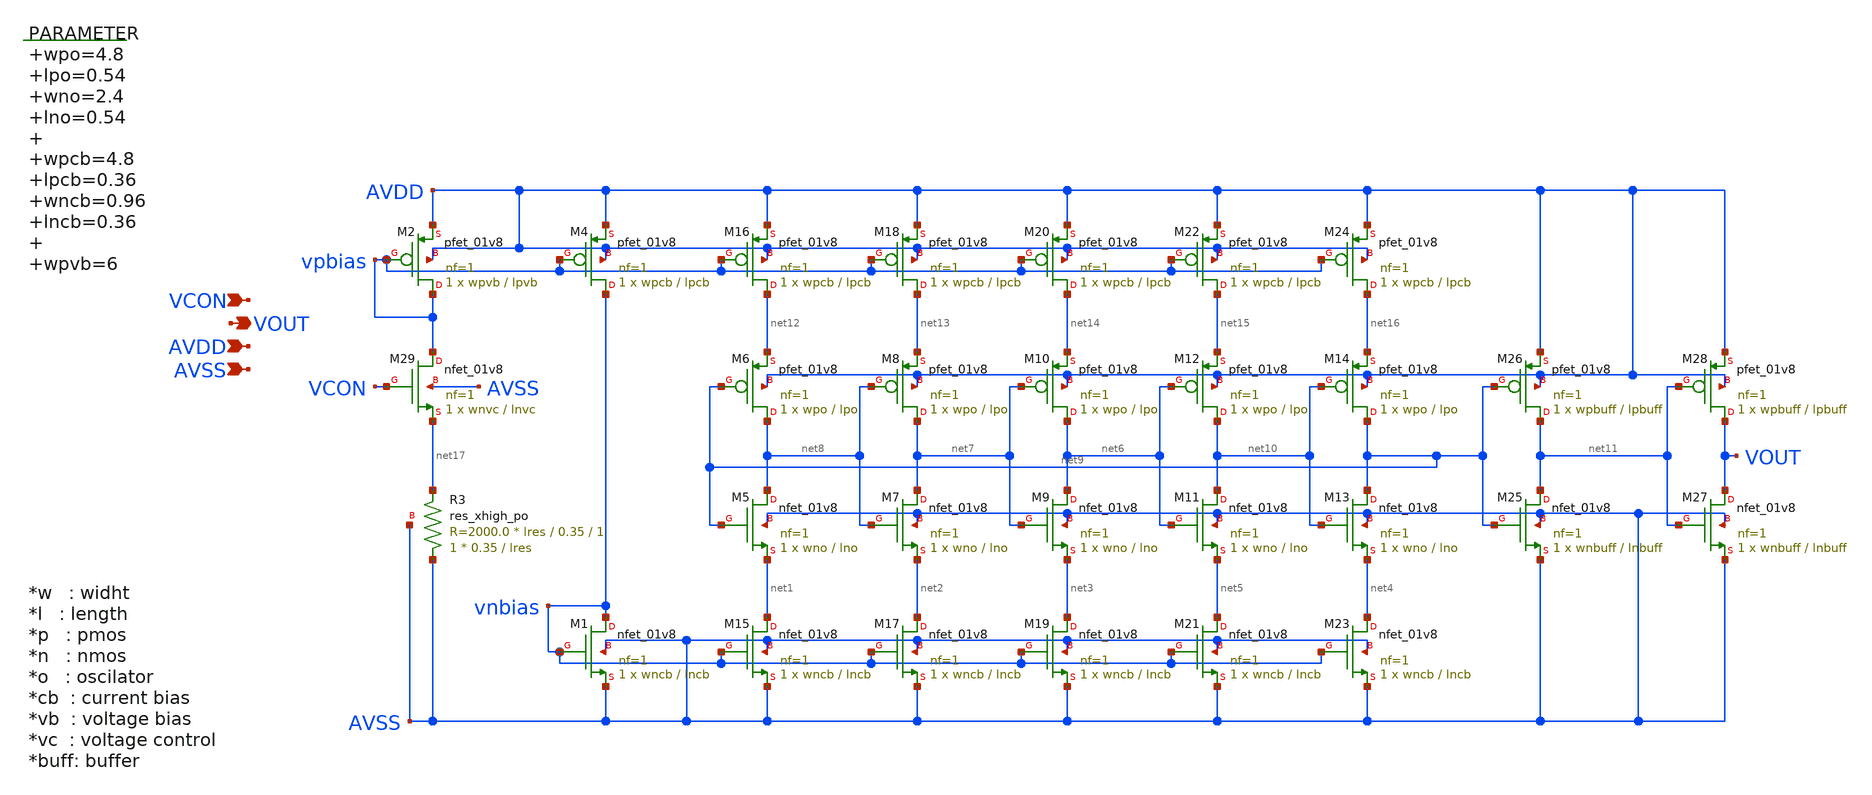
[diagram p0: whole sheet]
** sch_path: xschem/vco.sch
**.subckt vco VCON VOUT AVDD AVSS
*.ipin VCON
*.opin VOUT
*.ipin AVDD
*.ipin AVSS
.param wpo=4.8 lpo=0.54 wno=2.4 lno=0.54 wpcb=4.8 lpcb=0.36 wncb=0.96 lncb=0.36 wpvb=6 lpvb=0.9
+ wnvc=96 lnvc=0.9 wpbuff=4.8 lpbuff=0.18 wnbuff=1.2 lnbuff=0.18 lres=3.5

XM1 vnbias vnbias AVSS AVSS sky130_fd_pr__nfet_01v8 L=lncb W=wncb nf=1 ad='int((nf+1)/2) * W/nf * 0.29'
+ as='int((nf+2)/2) * W/nf * 0.29' pd='2*int((nf+1)/2) * (W/nf + 0.29)' ps='2*int((nf+2)/2) * (W/nf + 0.29)'
+ nrd='0.29 / W' nrs='0.29 / W' sa=0 sb=0 sd=0 mult=1 m=1
XM2 vpbias vpbias AVDD AVDD sky130_fd_pr__pfet_01v8 L=lpvb W=wpvb nf=1 ad='int((nf+1)/2) * W/nf * 0.29'
+ as='int((nf+2)/2) * W/nf * 0.29' pd='2*int((nf+1)/2) * (W/nf + 0.29)' ps='2*int((nf+2)/2) * (W/nf + 0.29)'
+ nrd='0.29 / W' nrs='0.29 / W' sa=0 sb=0 sd=0 mult=1 m=1
XM4 vnbias vpbias AVDD AVDD sky130_fd_pr__pfet_01v8 L=lpcb W=wpcb nf=1 ad='int((nf+1)/2) * W/nf * 0.29'
+ as='int((nf+2)/2) * W/nf * 0.29' pd='2*int((nf+1)/2) * (W/nf + 0.29)' ps='2*int((nf+2)/2) * (W/nf + 0.29)'
+ nrd='0.29 / W' nrs='0.29 / W' sa=0 sb=0 sd=0 mult=1 m=1
XM5 net8 net9 net1 AVSS sky130_fd_pr__nfet_01v8 L=lno W=wno nf=1 ad='int((nf+1)/2) * W/nf * 0.29' as='int((nf+2)/2) * W/nf * 0.29'
+ pd='2*int((nf+1)/2) * (W/nf + 0.29)' ps='2*int((nf+2)/2) * (W/nf + 0.29)' nrd='0.29 / W' nrs='0.29 / W'
+ sa=0 sb=0 sd=0 mult=1 m=1
XM6 net8 net9 net12 AVDD sky130_fd_pr__pfet_01v8 L=lpo W=wpo nf=1 ad='int((nf+1)/2) * W/nf * 0.29' as='int((nf+2)/2) * W/nf * 0.29'
+ pd='2*int((nf+1)/2) * (W/nf + 0.29)' ps='2*int((nf+2)/2) * (W/nf + 0.29)' nrd='0.29 / W' nrs='0.29 / W'
+ sa=0 sb=0 sd=0 mult=1 m=1
XM7 net7 net8 net2 AVSS sky130_fd_pr__nfet_01v8 L=lno W=wno nf=1 ad='int((nf+1)/2) * W/nf * 0.29' as='int((nf+2)/2) * W/nf * 0.29'
+ pd='2*int((nf+1)/2) * (W/nf + 0.29)' ps='2*int((nf+2)/2) * (W/nf + 0.29)' nrd='0.29 / W' nrs='0.29 / W'
+ sa=0 sb=0 sd=0 mult=1 m=1
XM8 net7 net8 net13 AVDD sky130_fd_pr__pfet_01v8 L=lpo W=wpo nf=1 ad='int((nf+1)/2) * W/nf * 0.29' as='int((nf+2)/2) * W/nf * 0.29'
+ pd='2*int((nf+1)/2) * (W/nf + 0.29)' ps='2*int((nf+2)/2) * (W/nf + 0.29)' nrd='0.29 / W' nrs='0.29 / W'
+ sa=0 sb=0 sd=0 mult=1 m=1
XM9 net6 net7 net3 AVSS sky130_fd_pr__nfet_01v8 L=lno W=wno nf=1 ad='int((nf+1)/2) * W/nf * 0.29' as='int((nf+2)/2) * W/nf * 0.29'
+ pd='2*int((nf+1)/2) * (W/nf + 0.29)' ps='2*int((nf+2)/2) * (W/nf + 0.29)' nrd='0.29 / W' nrs='0.29 / W'
+ sa=0 sb=0 sd=0 mult=1 m=1
XM10 net6 net7 net14 AVDD sky130_fd_pr__pfet_01v8 L=lpo W=wpo nf=1 ad='int((nf+1)/2) * W/nf * 0.29' as='int((nf+2)/2) * W/nf * 0.29'
+ pd='2*int((nf+1)/2) * (W/nf + 0.29)' ps='2*int((nf+2)/2) * (W/nf + 0.29)' nrd='0.29 / W' nrs='0.29 / W'
+ sa=0 sb=0 sd=0 mult=1 m=1
XM11 net10 net6 net5 AVSS sky130_fd_pr__nfet_01v8 L=lno W=wno nf=1 ad='int((nf+1)/2) * W/nf * 0.29' as='int((nf+2)/2) * W/nf * 0.29'
+ pd='2*int((nf+1)/2) * (W/nf + 0.29)' ps='2*int((nf+2)/2) * (W/nf + 0.29)' nrd='0.29 / W' nrs='0.29 / W'
+ sa=0 sb=0 sd=0 mult=1 m=1
XM12 net10 net6 net15 AVDD sky130_fd_pr__pfet_01v8 L=lpo W=wpo nf=1 ad='int((nf+1)/2) * W/nf * 0.29'
+ as='int((nf+2)/2) * W/nf * 0.29' pd='2*int((nf+1)/2) * (W/nf + 0.29)' ps='2*int((nf+2)/2) * (W/nf + 0.29)'
+ nrd='0.29 / W' nrs='0.29 / W' sa=0 sb=0 sd=0 mult=1 m=1
XM13 net9 net10 net4 AVSS sky130_fd_pr__nfet_01v8 L=lno W=wno nf=1 ad='int((nf+1)/2) * W/nf * 0.29' as='int((nf+2)/2) * W/nf * 0.29'
+ pd='2*int((nf+1)/2) * (W/nf + 0.29)' ps='2*int((nf+2)/2) * (W/nf + 0.29)' nrd='0.29 / W' nrs='0.29 / W'
+ sa=0 sb=0 sd=0 mult=1 m=1
XM14 net9 net10 net16 AVDD sky130_fd_pr__pfet_01v8 L=lpo W=wpo nf=1 ad='int((nf+1)/2) * W/nf * 0.29'
+ as='int((nf+2)/2) * W/nf * 0.29' pd='2*int((nf+1)/2) * (W/nf + 0.29)' ps='2*int((nf+2)/2) * (W/nf + 0.29)'
+ nrd='0.29 / W' nrs='0.29 / W' sa=0 sb=0 sd=0 mult=1 m=1
XM16 net12 vpbias AVDD AVDD sky130_fd_pr__pfet_01v8 L=lpcb W=wpcb nf=1 ad='int((nf+1)/2) * W/nf * 0.29'
+ as='int((nf+2)/2) * W/nf * 0.29' pd='2*int((nf+1)/2) * (W/nf + 0.29)' ps='2*int((nf+2)/2) * (W/nf + 0.29)'
+ nrd='0.29 / W' nrs='0.29 / W' sa=0 sb=0 sd=0 mult=1 m=1
XM18 net13 vpbias AVDD AVDD sky130_fd_pr__pfet_01v8 L=lpcb W=wpcb nf=1 ad='int((nf+1)/2) * W/nf * 0.29'
+ as='int((nf+2)/2) * W/nf * 0.29' pd='2*int((nf+1)/2) * (W/nf + 0.29)' ps='2*int((nf+2)/2) * (W/nf + 0.29)'
+ nrd='0.29 / W' nrs='0.29 / W' sa=0 sb=0 sd=0 mult=1 m=1
XM20 net14 vpbias AVDD AVDD sky130_fd_pr__pfet_01v8 L=lpcb W=wpcb nf=1 ad='int((nf+1)/2) * W/nf * 0.29'
+ as='int((nf+2)/2) * W/nf * 0.29' pd='2*int((nf+1)/2) * (W/nf + 0.29)' ps='2*int((nf+2)/2) * (W/nf + 0.29)'
+ nrd='0.29 / W' nrs='0.29 / W' sa=0 sb=0 sd=0 mult=1 m=1
XM22 net15 vpbias AVDD AVDD sky130_fd_pr__pfet_01v8 L=lpcb W=wpcb nf=1 ad='int((nf+1)/2) * W/nf * 0.29'
+ as='int((nf+2)/2) * W/nf * 0.29' pd='2*int((nf+1)/2) * (W/nf + 0.29)' ps='2*int((nf+2)/2) * (W/nf + 0.29)'
+ nrd='0.29 / W' nrs='0.29 / W' sa=0 sb=0 sd=0 mult=1 m=1
XM24 net16 vpbias AVDD AVDD sky130_fd_pr__pfet_01v8 L=lpcb W=wpcb nf=1 ad='int((nf+1)/2) * W/nf * 0.29'
+ as='int((nf+2)/2) * W/nf * 0.29' pd='2*int((nf+1)/2) * (W/nf + 0.29)' ps='2*int((nf+2)/2) * (W/nf + 0.29)'
+ nrd='0.29 / W' nrs='0.29 / W' sa=0 sb=0 sd=0 mult=1 m=1
XM25 net11 net9 AVSS AVSS sky130_fd_pr__nfet_01v8 L=lnbuff W=wnbuff nf=1 ad='int((nf+1)/2) * W/nf * 0.29'
+ as='int((nf+2)/2) * W/nf * 0.29' pd='2*int((nf+1)/2) * (W/nf + 0.29)' ps='2*int((nf+2)/2) * (W/nf + 0.29)'
+ nrd='0.29 / W' nrs='0.29 / W' sa=0 sb=0 sd=0 mult=1 m=1
XM26 net11 net9 AVDD AVDD sky130_fd_pr__pfet_01v8 L=lpbuff W=wpbuff nf=1 ad='int((nf+1)/2) * W/nf * 0.29'
+ as='int((nf+2)/2) * W/nf * 0.29' pd='2*int((nf+1)/2) * (W/nf + 0.29)' ps='2*int((nf+2)/2) * (W/nf + 0.29)'
+ nrd='0.29 / W' nrs='0.29 / W' sa=0 sb=0 sd=0 mult=1 m=1
XM27 VOUT net11 AVSS AVSS sky130_fd_pr__nfet_01v8 L=lnbuff W=wnbuff nf=1 ad='int((nf+1)/2) * W/nf * 0.29'
+ as='int((nf+2)/2) * W/nf * 0.29' pd='2*int((nf+1)/2) * (W/nf + 0.29)' ps='2*int((nf+2)/2) * (W/nf + 0.29)'
+ nrd='0.29 / W' nrs='0.29 / W' sa=0 sb=0 sd=0 mult=1 m=1
XM28 VOUT net11 AVDD AVDD sky130_fd_pr__pfet_01v8 L=lpbuff W=wpbuff nf=1 ad='int((nf+1)/2) * W/nf * 0.29'
+ as='int((nf+2)/2) * W/nf * 0.29' pd='2*int((nf+1)/2) * (W/nf + 0.29)' ps='2*int((nf+2)/2) * (W/nf + 0.29)'
+ nrd='0.29 / W' nrs='0.29 / W' sa=0 sb=0 sd=0 mult=1 m=1
XM15 net1 vnbias AVSS AVSS sky130_fd_pr__nfet_01v8 L=lncb W=wncb nf=1 ad='int((nf+1)/2) * W/nf * 0.29'
+ as='int((nf+2)/2) * W/nf * 0.29' pd='2*int((nf+1)/2) * (W/nf + 0.29)' ps='2*int((nf+2)/2) * (W/nf + 0.29)'
+ nrd='0.29 / W' nrs='0.29 / W' sa=0 sb=0 sd=0 mult=1 m=1
XM17 net2 vnbias AVSS AVSS sky130_fd_pr__nfet_01v8 L=lncb W=wncb nf=1 ad='int((nf+1)/2) * W/nf * 0.29'
+ as='int((nf+2)/2) * W/nf * 0.29' pd='2*int((nf+1)/2) * (W/nf + 0.29)' ps='2*int((nf+2)/2) * (W/nf + 0.29)'
+ nrd='0.29 / W' nrs='0.29 / W' sa=0 sb=0 sd=0 mult=1 m=1
XM19 net3 vnbias AVSS AVSS sky130_fd_pr__nfet_01v8 L=lncb W=wncb nf=1 ad='int((nf+1)/2) * W/nf * 0.29'
+ as='int((nf+2)/2) * W/nf * 0.29' pd='2*int((nf+1)/2) * (W/nf + 0.29)' ps='2*int((nf+2)/2) * (W/nf + 0.29)'
+ nrd='0.29 / W' nrs='0.29 / W' sa=0 sb=0 sd=0 mult=1 m=1
XM21 net5 vnbias AVSS AVSS sky130_fd_pr__nfet_01v8 L=lncb W=wncb nf=1 ad='int((nf+1)/2) * W/nf * 0.29'
+ as='int((nf+2)/2) * W/nf * 0.29' pd='2*int((nf+1)/2) * (W/nf + 0.29)' ps='2*int((nf+2)/2) * (W/nf + 0.29)'
+ nrd='0.29 / W' nrs='0.29 / W' sa=0 sb=0 sd=0 mult=1 m=1
XM23 net4 vnbias AVSS AVSS sky130_fd_pr__nfet_01v8 L=lncb W=wncb nf=1 ad='int((nf+1)/2) * W/nf * 0.29'
+ as='int((nf+2)/2) * W/nf * 0.29' pd='2*int((nf+1)/2) * (W/nf + 0.29)' ps='2*int((nf+2)/2) * (W/nf + 0.29)'
+ nrd='0.29 / W' nrs='0.29 / W' sa=0 sb=0 sd=0 mult=1 m=1
XR3 AVSS net17 AVSS sky130_fd_pr__res_xhigh_po W=0.35 L=lres mult=1 m=1
XM29 vpbias VCON net17 AVSS sky130_fd_pr__nfet_01v8 L=lnvc W=wnvc nf=1 ad='int((nf+1)/2) * W/nf * 0.29'
+ as='int((nf+2)/2) * W/nf * 0.29' pd='2*int((nf+1)/2) * (W/nf + 0.29)' ps='2*int((nf+2)/2) * (W/nf + 0.29)'
+ nrd='0.29 / W' nrs='0.29 / W' sa=0 sb=0 sd=0 mult=1 m=1
**.ends
.end
